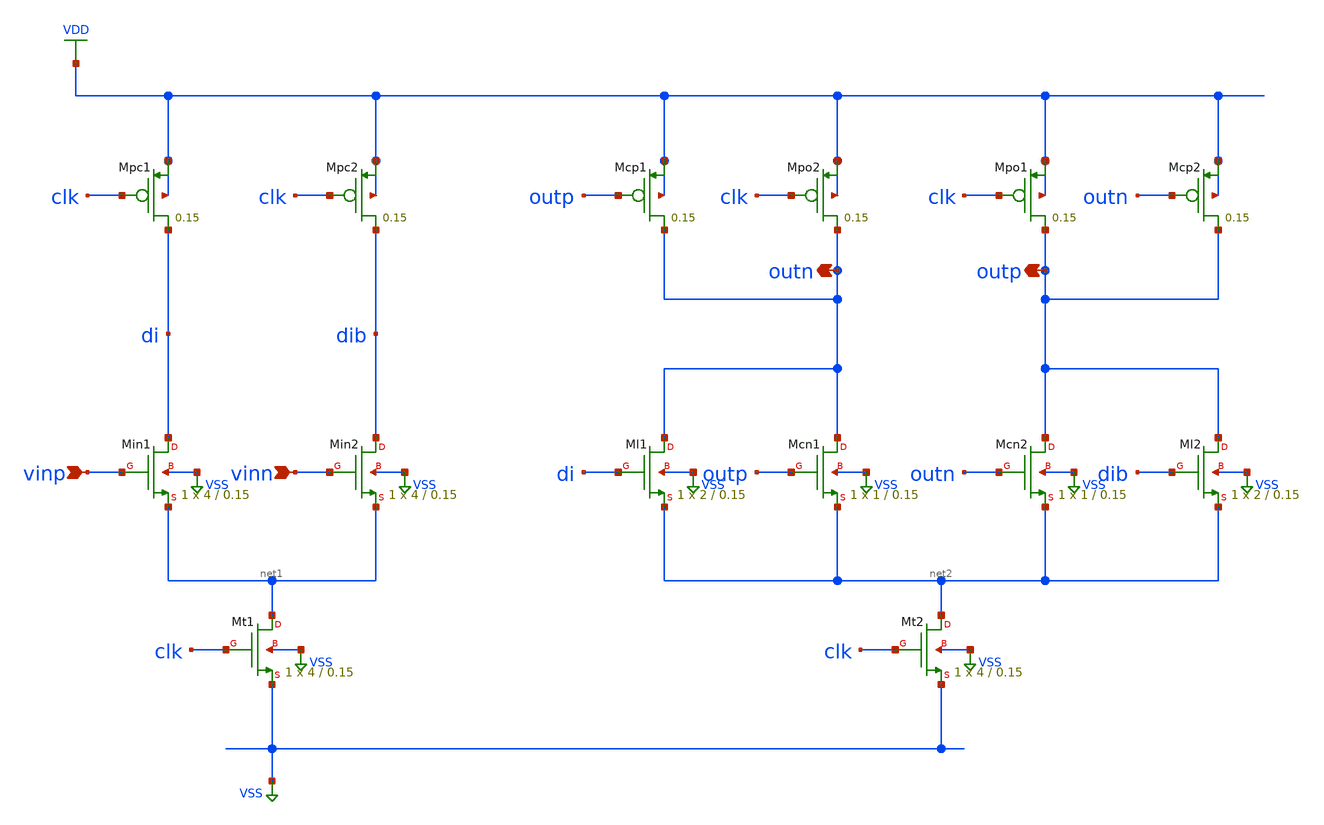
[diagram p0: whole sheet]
** sch_path: eda/hero/schematics/double_tail.sch
**.subckt double_tail vinp vinn outn outp
*.ipin vinp
*.ipin vinn
*.opin outn
*.opin outp
XMpc1 di clk VDD VDD sky130_fd_pr__sky130_fd_pr__pfet_01v8 L=0.15 W=2 nrd='0.29 / W' nrs='0.29 / W' sa=0
+ sb=0 sd=0 mult=1 m=1
XMpc2 dib clk VDD VDD sky130_fd_pr__sky130_fd_pr__pfet_01v8 L=0.15 W=2 nrd='0.29 / W' nrs='0.29 / W'
+ sa=0 sb=0 sd=0 mult=1 m=1
XMin1 di vinp net1 VSS sky130_fd_pr__sky130_fd_pr__nfet_01v8 L=0.15 W=4 nrd='0.29 / W' nrs='0.29 / W'
+ sa=0 sb=0 sd=0 mult=1 m=1
XMin2 dib vinn net1 VSS sky130_fd_pr__sky130_fd_pr__nfet_01v8 L=0.15 W=4 nrd='0.29 / W' nrs='0.29 / W'
+ sa=0 sb=0 sd=0 mult=1 m=1
XMt1 net1 clk VSS VSS sky130_fd_pr__sky130_fd_pr__nfet_01v8 L=0.15 W=4 nrd='0.29 / W' nrs='0.29 / W'
+ sa=0 sb=0 sd=0 mult=1 m=1
XMcp1 outn outp VDD VDD sky130_fd_pr__sky130_fd_pr__pfet_01v8 L=0.15 W=2 nrd='0.29 / W' nrs='0.29 / W'
+ sa=0 sb=0 sd=0 mult=1 m=1
XMpo2 outn clk VDD VDD sky130_fd_pr__sky130_fd_pr__pfet_01v8 L=0.15 W=2 nrd='0.29 / W' nrs='0.29 / W'
+ sa=0 sb=0 sd=0 mult=1 m=1
XMpo1 outp clk VDD VDD sky130_fd_pr__sky130_fd_pr__pfet_01v8 L=0.15 W=2 nrd='0.29 / W' nrs='0.29 / W'
+ sa=0 sb=0 sd=0 mult=1 m=1
XMcp2 outp outn VDD VDD sky130_fd_pr__sky130_fd_pr__pfet_01v8 L=0.15 W=2 nrd='0.29 / W' nrs='0.29 / W'
+ sa=0 sb=0 sd=0 mult=1 m=1
XMl1 outn di net2 VSS sky130_fd_pr__sky130_fd_pr__nfet_01v8 L=0.15 W=2 nrd='0.29 / W' nrs='0.29 / W'
+ sa=0 sb=0 sd=0 mult=1 m=1
XMcn1 outn outp net2 VSS sky130_fd_pr__sky130_fd_pr__nfet_01v8 L=0.15 W=1 nrd='0.29 / W' nrs='0.29 / W'
+ sa=0 sb=0 sd=0 mult=1 m=1
XMcn2 outp outn net2 VSS sky130_fd_pr__sky130_fd_pr__nfet_01v8 L=0.15 W=1 nrd='0.29 / W' nrs='0.29 / W'
+ sa=0 sb=0 sd=0 mult=1 m=1
XMl2 outp dib net2 VSS sky130_fd_pr__sky130_fd_pr__nfet_01v8 L=0.15 W=2 nrd='0.29 / W' nrs='0.29 / W'
+ sa=0 sb=0 sd=0 mult=1 m=1
XMt2 net2 clk VSS VSS sky130_fd_pr__sky130_fd_pr__nfet_01v8 L=0.15 W=4 nrd='0.29 / W' nrs='0.29 / W'
+ sa=0 sb=0 sd=0 mult=1 m=1
**.ends
.GLOBAL VSS
.GLOBAL VDD
.end
